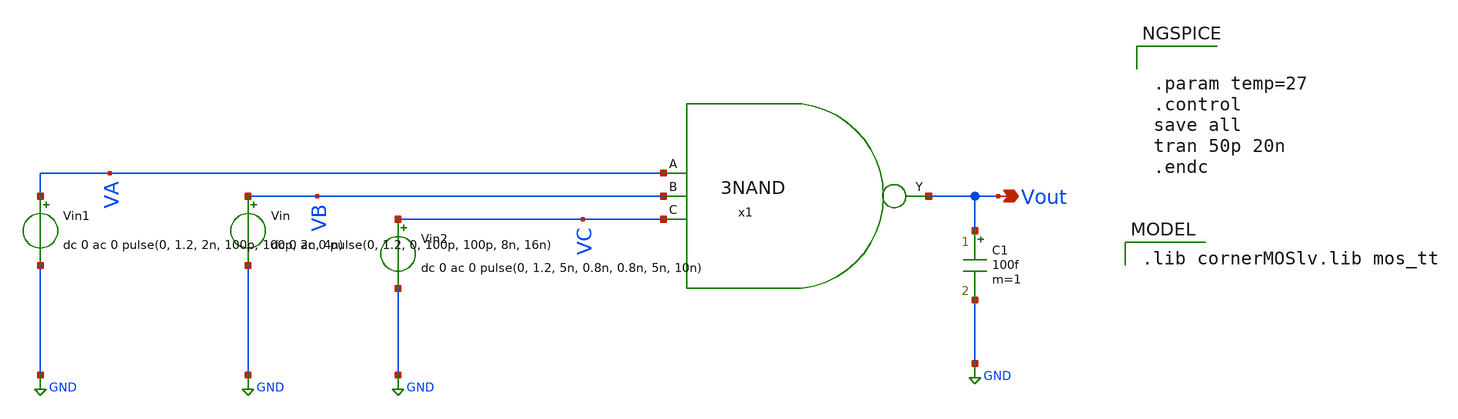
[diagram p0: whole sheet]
** sch_path: Team 1 Design/design_data/xschem/3_Input_NAND/3NAND_tb.sch
**.subckt 3NAND_tb Vout
*.opin Vout
Vin VB GND dc 0 ac 0 pulse(0, 1.2, 0, 100p, 100p, 8n, 16n)
Vin1 VA GND dc 0 ac 0 pulse(0, 1.2, 2n, 100p, 100p, 2n, 4n)
C1 Vout GND 100f m=1
x1 Vout VA VB VC 3NAND
Vin2 VC GND dc 0 ac 0 pulse(0, 1.2, 5n, 0.8n, 0.8n, 5n, 10n)
**** begin user architecture code
 .lib cornerMOSlv.lib mos_tt



.param temp=27
.control
save all
tran 50p 20n
.endc


**** end user architecture code
**.ends

* expanding   symbol:  /foss/designs/Team2/3NAND/3NAND.sym # of pins=4
** sym_path: Team 1 Design/design_data/xschem/3_Input_NAND/3NAND.sym
** sch_path: Team 1 Design/design_data/xschem/3_Input_NAND/3NAND.sch
.subckt 3NAND Y A B C
*.ipin A
*.ipin B
*.ipin C
*.opin Y
XM1 Y A Vdd Vdd sg13_lv_pmos w=2u l=0.13u ng=1 m=1 mm_ok=1
XM2 Y B Vdd Vdd sg13_lv_pmos w=2u l=0.13u ng=1 m=1 mm_ok=1
XM3 Y C Vdd Vdd sg13_lv_pmos w=2u l=0.13u ng=1 m=1 mm_ok=1
XM4 Y A net1 GND sg13_lv_nmos w=1u l=0.13u ng=1 m=1 mm_ok=1
XM5 net1 B net2 GND sg13_lv_nmos w=1u l=0.13u ng=1 m=1 mm_ok=1
XM6 net2 C GND GND sg13_lv_nmos w=1u l=0.13u ng=1 m=1 mm_ok=1
V1 Vdd GND 1.2
.ends

.GLOBAL GND
.end
